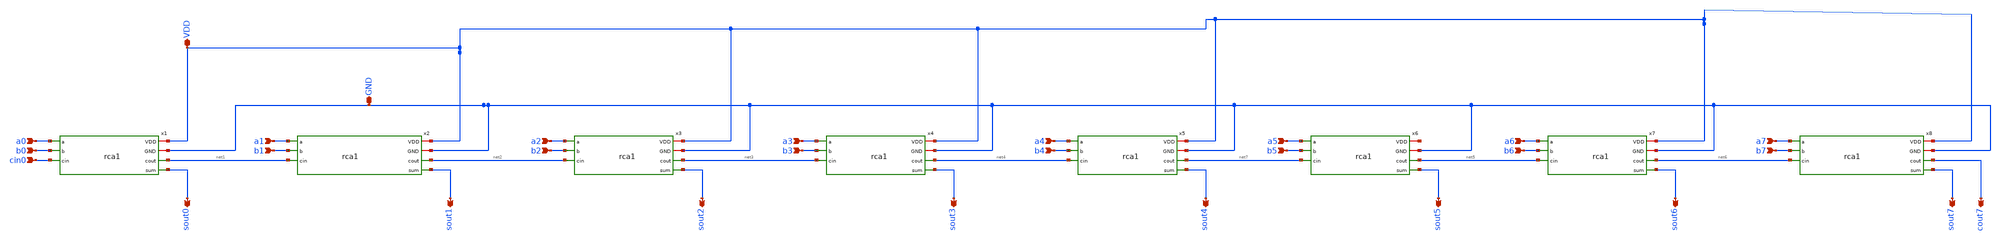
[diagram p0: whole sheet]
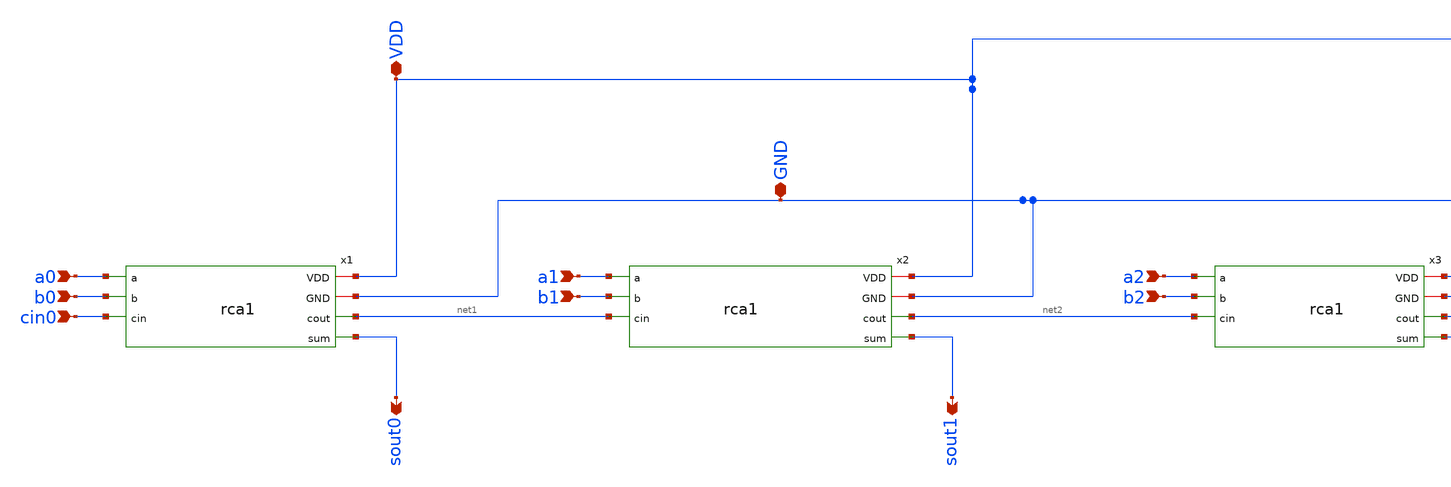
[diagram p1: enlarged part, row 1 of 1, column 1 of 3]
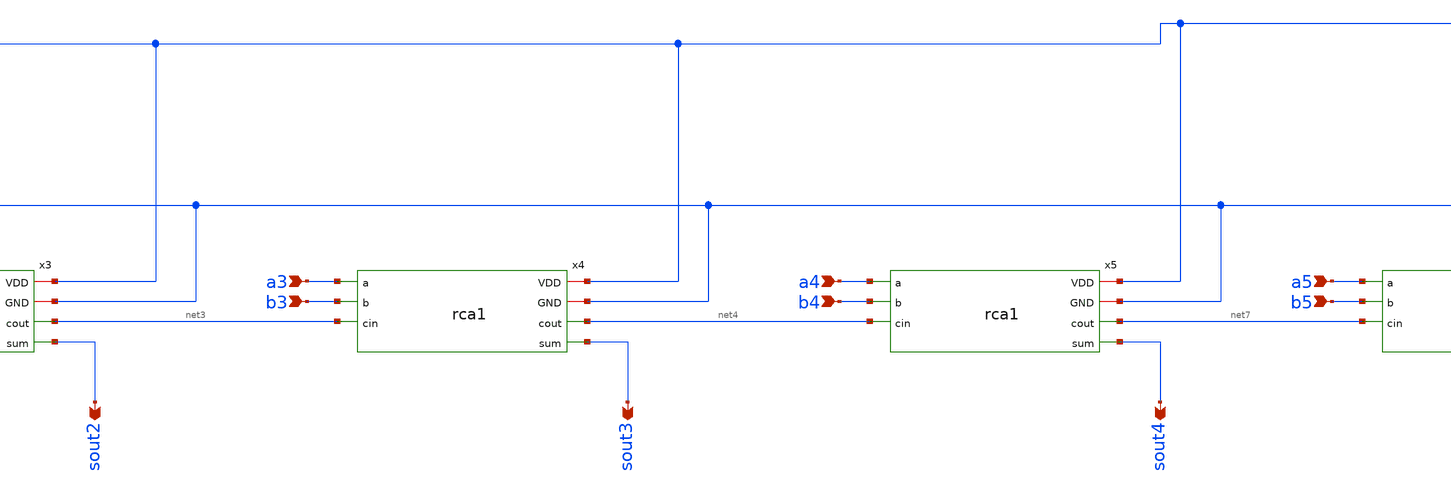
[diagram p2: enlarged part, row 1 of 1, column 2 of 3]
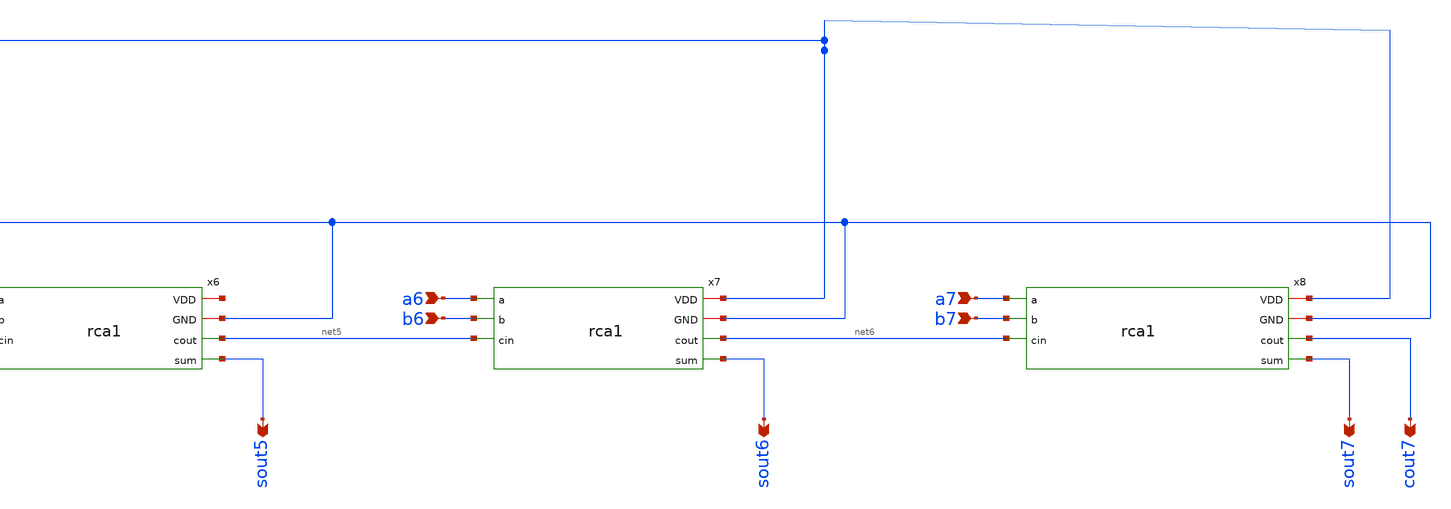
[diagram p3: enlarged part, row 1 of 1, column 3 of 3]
** sch_path: assignments/assignment8/rca8.sch
**.subckt rca8 a0 b0 cin0 sout0 VDD GND a1 b1 sout1 a2 b2 sout2 a3 b3 sout3 a4 b4 sout4 a5 b5 sout5
*+ a6 b6 sout6 a7 b7 sout7 cout7
*.ipin a0
*.ipin b0
*.ipin cin0
*.opin sout0
*.iopin VDD
*.iopin GND
*.ipin a1
*.ipin b1
*.opin sout1
*.ipin a2
*.ipin b2
*.opin sout2
*.ipin a3
*.ipin b3
*.opin sout3
*.ipin a4
*.ipin b4
*.opin sout4
*.ipin a5
*.ipin b5
*.opin sout5
*.ipin a6
*.ipin b6
*.opin sout6
*.ipin a7
*.ipin b7
*.opin sout7
*.opin cout7
x1 VDD a0 b0 cin0 GND net1 sout0 rca1
x2 VDD a1 b1 net1 GND net2 sout1 rca1
x3 VDD a2 b2 net2 GND net3 sout2 rca1
x4 VDD a3 b3 net3 GND net4 sout3 rca1
x5 VDD a4 b4 net4 GND net7 sout4 rca1
x6 net8 a5 b5 net7 GND net5 sout5 rca1
x7 VDD a6 b6 net5 GND net6 sout6 rca1
x8 VDD a7 b7 net6 GND cout7 sout7 rca1
**.ends
.end
